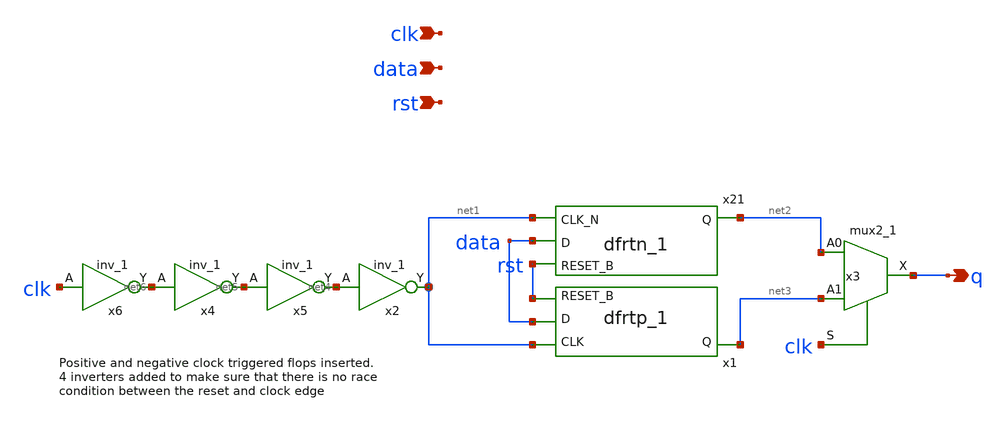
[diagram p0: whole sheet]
** sch_path: xschem/tryandtest/deff_rst.sch
**.subckt deff_rst clk data q rst
*.ipin clk
*.ipin data
*.opin q
*.ipin rst
x3 net2 net3 clk GND GND VDD VDD q sky130_fd_sc_lp__mux2_1
x21 net1 data rst GND GND VDD VDD net2 sky130_fd_sc_lp__dfrtn_1
x2 net4 GND GND VDD VDD net1 sky130_fd_sc_lp__inv_1
x5 net5 GND GND VDD VDD net4 sky130_fd_sc_lp__inv_1
x1 net1 data rst GND GND VDD VDD net3 sky130_fd_sc_lp__dfrtp_1
x4 net6 GND GND VDD VDD net5 sky130_fd_sc_lp__inv_1
x6 clk GND GND VDD VDD net6 sky130_fd_sc_lp__inv_1
**.ends
.end
